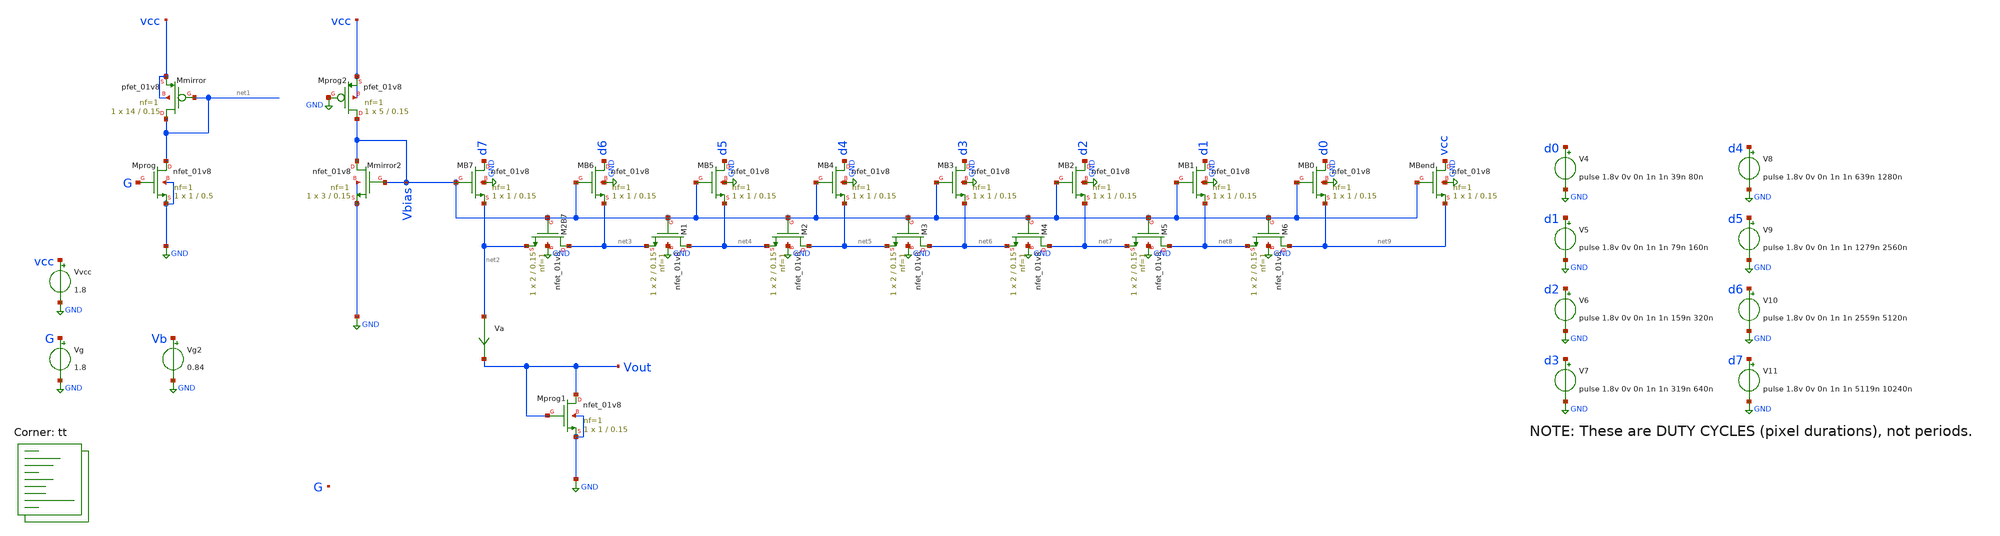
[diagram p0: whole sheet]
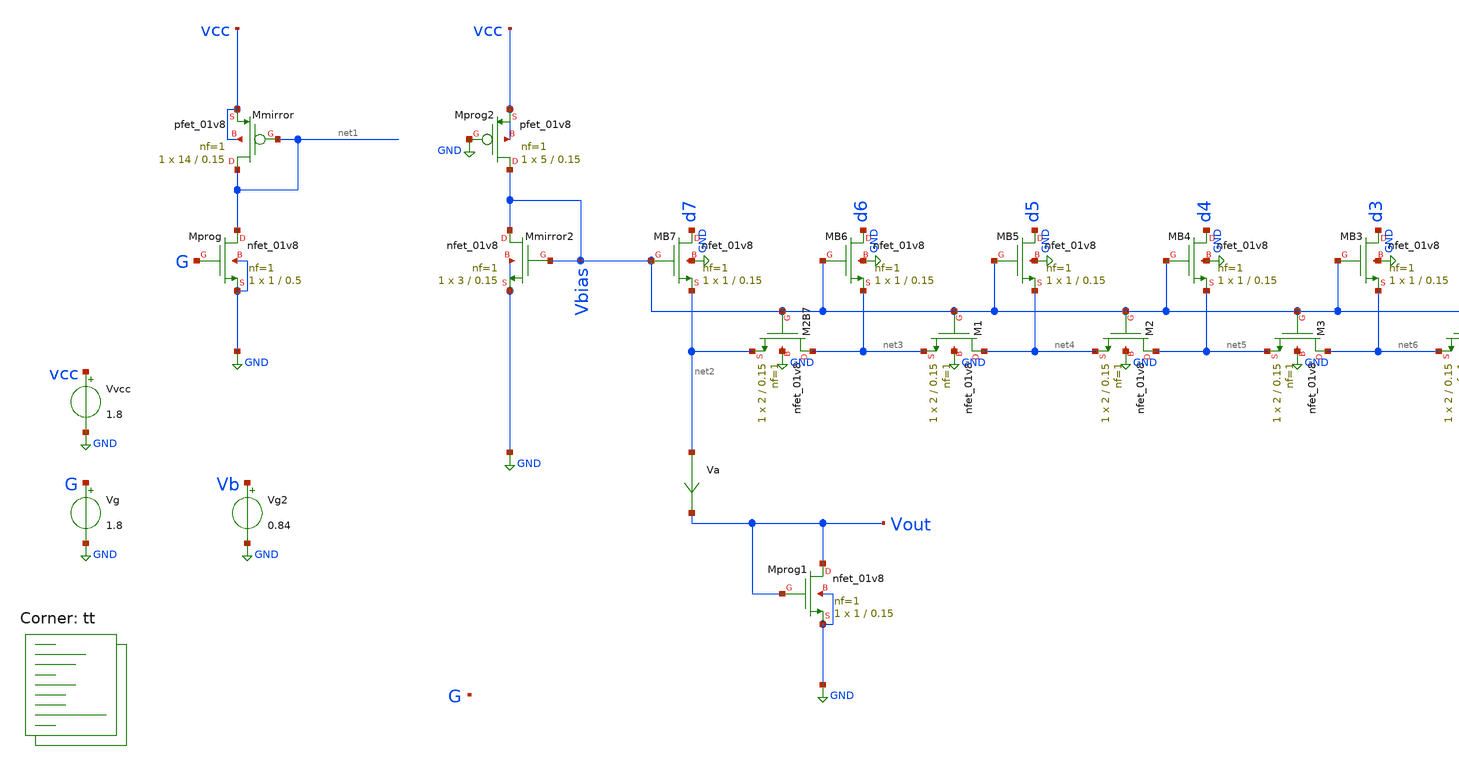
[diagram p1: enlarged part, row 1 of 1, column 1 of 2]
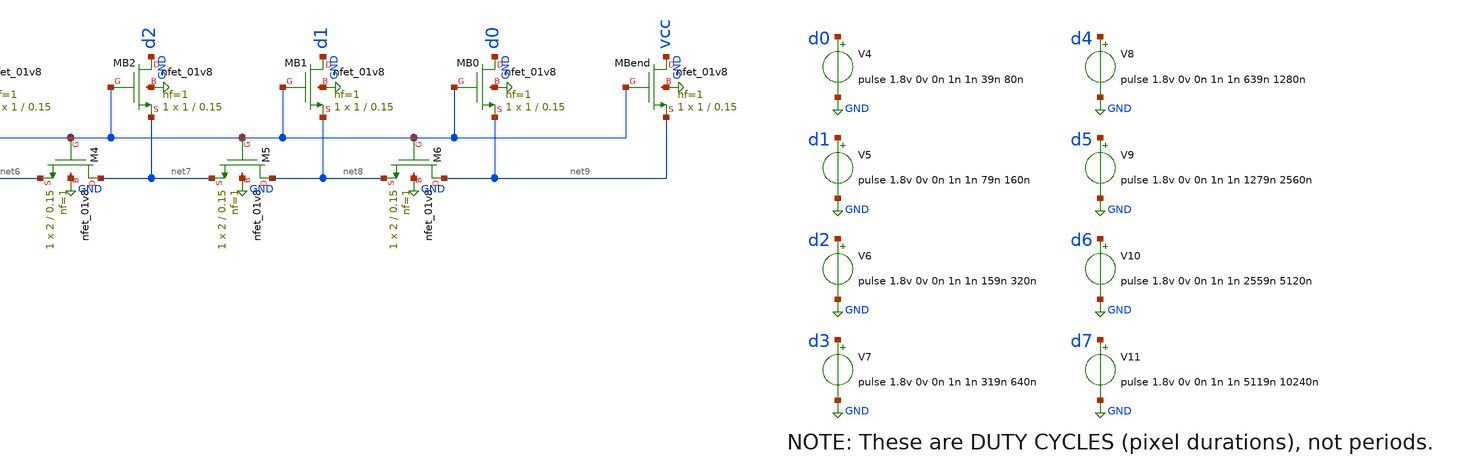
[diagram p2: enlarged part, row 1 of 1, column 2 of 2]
** sch_path: xschem/09-w2w.sch
**.subckt 09-w2w
Vvcc vcc GND 1.8
Vg2 Vb GND 0.84
Vg G GND 1.8
XMprog net1 G GND GND sky130_fd_pr__nfet_01v8 L=0.5 W=1 nf=1 ad='int((nf+1)/2) * W/nf * 0.29' as='int((nf+2)/2) * W/nf * 0.29'
+ pd='2*int((nf+1)/2) * (W/nf + 0.29)' ps='2*int((nf+2)/2) * (W/nf + 0.29)' nrd='0.29 / W' nrs='0.29 / W'
+ sa=0 sb=0 sd=0 mult=1 m=1
XMmirror net1 net1 vcc vcc sky130_fd_pr__pfet_01v8 L=0.15 W=14 nf=1 ad='int((nf+1)/2) * W/nf * 0.29'
+ as='int((nf+2)/2) * W/nf * 0.29' pd='2*int((nf+1)/2) * (W/nf + 0.29)' ps='2*int((nf+2)/2) * (W/nf + 0.29)'
+ nrd='0.29 / W' nrs='0.29 / W' sa=0 sb=0 sd=0 mult=1 m=1
XMprog2 Vbias GND vcc vcc sky130_fd_pr__pfet_01v8 L=0.15 W=5 nf=1 ad='int((nf+1)/2) * W/nf * 0.29' as='int((nf+2)/2) * W/nf * 0.29'
+ pd='2*int((nf+1)/2) * (W/nf + 0.29)' ps='2*int((nf+2)/2) * (W/nf + 0.29)' nrd='0.29 / W' nrs='0.29 / W'
+ sa=0 sb=0 sd=0 mult=1 m=1
XMmirror2 Vbias Vbias GND GND sky130_fd_pr__nfet_01v8 L=0.15 W=3 nf=1 ad='int((nf+1)/2) * W/nf * 0.29'
+ as='int((nf+2)/2) * W/nf * 0.29' pd='2*int((nf+1)/2) * (W/nf + 0.29)' ps='2*int((nf+2)/2) * (W/nf + 0.29)'
+ nrd='0.29 / W' nrs='0.29 / W' sa=0 sb=0 sd=0 mult=1 m=1
XMB7 d7 Vbias net2 GND sky130_fd_pr__nfet_01v8 L=0.15 W=1 nf=1 ad='int((nf+1)/2) * W/nf * 0.29' as='int((nf+2)/2) * W/nf * 0.29'
+ pd='2*int((nf+1)/2) * (W/nf + 0.29)' ps='2*int((nf+2)/2) * (W/nf + 0.29)' nrd='0.29 / W' nrs='0.29 / W'
+ sa=0 sb=0 sd=0 mult=1 m=1
XM2B7 net3 Vbias net2 GND sky130_fd_pr__nfet_01v8 L=0.15 W=2 nf=1 ad='int((nf+1)/2) * W/nf * 0.29' as='int((nf+2)/2) * W/nf * 0.29'
+ pd='2*int((nf+1)/2) * (W/nf + 0.29)' ps='2*int((nf+2)/2) * (W/nf + 0.29)' nrd='0.29 / W' nrs='0.29 / W'
+ sa=0 sb=0 sd=0 mult=1 m=1
XMB1 d1 Vbias net8 GND sky130_fd_pr__nfet_01v8 L=0.15 W=1 nf=1 ad='int((nf+1)/2) * W/nf * 0.29' as='int((nf+2)/2) * W/nf * 0.29'
+ pd='2*int((nf+1)/2) * (W/nf + 0.29)' ps='2*int((nf+2)/2) * (W/nf + 0.29)' nrd='0.29 / W' nrs='0.29 / W'
+ sa=0 sb=0 sd=0 mult=1 m=1
XM1 net4 Vbias net3 GND sky130_fd_pr__nfet_01v8 L=0.15 W=2 nf=1 ad='int((nf+1)/2) * W/nf * 0.29' as='int((nf+2)/2) * W/nf * 0.29'
+ pd='2*int((nf+1)/2) * (W/nf + 0.29)' ps='2*int((nf+2)/2) * (W/nf + 0.29)' nrd='0.29 / W' nrs='0.29 / W'
+ sa=0 sb=0 sd=0 mult=1 m=1
XMB2 d2 Vbias net7 GND sky130_fd_pr__nfet_01v8 L=0.15 W=1 nf=1 ad='int((nf+1)/2) * W/nf * 0.29' as='int((nf+2)/2) * W/nf * 0.29'
+ pd='2*int((nf+1)/2) * (W/nf + 0.29)' ps='2*int((nf+2)/2) * (W/nf + 0.29)' nrd='0.29 / W' nrs='0.29 / W'
+ sa=0 sb=0 sd=0 mult=1 m=1
XM2 net5 Vbias net4 GND sky130_fd_pr__nfet_01v8 L=0.15 W=2 nf=1 ad='int((nf+1)/2) * W/nf * 0.29' as='int((nf+2)/2) * W/nf * 0.29'
+ pd='2*int((nf+1)/2) * (W/nf + 0.29)' ps='2*int((nf+2)/2) * (W/nf + 0.29)' nrd='0.29 / W' nrs='0.29 / W'
+ sa=0 sb=0 sd=0 mult=1 m=1
XMB3 d3 Vbias net6 GND sky130_fd_pr__nfet_01v8 L=0.15 W=1 nf=1 ad='int((nf+1)/2) * W/nf * 0.29' as='int((nf+2)/2) * W/nf * 0.29'
+ pd='2*int((nf+1)/2) * (W/nf + 0.29)' ps='2*int((nf+2)/2) * (W/nf + 0.29)' nrd='0.29 / W' nrs='0.29 / W'
+ sa=0 sb=0 sd=0 mult=1 m=1
XM3 net6 Vbias net5 GND sky130_fd_pr__nfet_01v8 L=0.15 W=2 nf=1 ad='int((nf+1)/2) * W/nf * 0.29' as='int((nf+2)/2) * W/nf * 0.29'
+ pd='2*int((nf+1)/2) * (W/nf + 0.29)' ps='2*int((nf+2)/2) * (W/nf + 0.29)' nrd='0.29 / W' nrs='0.29 / W'
+ sa=0 sb=0 sd=0 mult=1 m=1
XMB4 d4 Vbias net5 GND sky130_fd_pr__nfet_01v8 L=0.15 W=1 nf=1 ad='int((nf+1)/2) * W/nf * 0.29' as='int((nf+2)/2) * W/nf * 0.29'
+ pd='2*int((nf+1)/2) * (W/nf + 0.29)' ps='2*int((nf+2)/2) * (W/nf + 0.29)' nrd='0.29 / W' nrs='0.29 / W'
+ sa=0 sb=0 sd=0 mult=1 m=1
XM4 net7 Vbias net6 GND sky130_fd_pr__nfet_01v8 L=0.15 W=2 nf=1 ad='int((nf+1)/2) * W/nf * 0.29' as='int((nf+2)/2) * W/nf * 0.29'
+ pd='2*int((nf+1)/2) * (W/nf + 0.29)' ps='2*int((nf+2)/2) * (W/nf + 0.29)' nrd='0.29 / W' nrs='0.29 / W'
+ sa=0 sb=0 sd=0 mult=1 m=1
XMB5 d5 Vbias net4 GND sky130_fd_pr__nfet_01v8 L=0.15 W=1 nf=1 ad='int((nf+1)/2) * W/nf * 0.29' as='int((nf+2)/2) * W/nf * 0.29'
+ pd='2*int((nf+1)/2) * (W/nf + 0.29)' ps='2*int((nf+2)/2) * (W/nf + 0.29)' nrd='0.29 / W' nrs='0.29 / W'
+ sa=0 sb=0 sd=0 mult=1 m=1
XM5 net8 Vbias net7 GND sky130_fd_pr__nfet_01v8 L=0.15 W=2 nf=1 ad='int((nf+1)/2) * W/nf * 0.29' as='int((nf+2)/2) * W/nf * 0.29'
+ pd='2*int((nf+1)/2) * (W/nf + 0.29)' ps='2*int((nf+2)/2) * (W/nf + 0.29)' nrd='0.29 / W' nrs='0.29 / W'
+ sa=0 sb=0 sd=0 mult=1 m=1
XMB6 d6 Vbias net3 GND sky130_fd_pr__nfet_01v8 L=0.15 W=1 nf=1 ad='int((nf+1)/2) * W/nf * 0.29' as='int((nf+2)/2) * W/nf * 0.29'
+ pd='2*int((nf+1)/2) * (W/nf + 0.29)' ps='2*int((nf+2)/2) * (W/nf + 0.29)' nrd='0.29 / W' nrs='0.29 / W'
+ sa=0 sb=0 sd=0 mult=1 m=1
XM6 net9 Vbias net8 GND sky130_fd_pr__nfet_01v8 L=0.15 W=2 nf=1 ad='int((nf+1)/2) * W/nf * 0.29' as='int((nf+2)/2) * W/nf * 0.29'
+ pd='2*int((nf+1)/2) * (W/nf + 0.29)' ps='2*int((nf+2)/2) * (W/nf + 0.29)' nrd='0.29 / W' nrs='0.29 / W'
+ sa=0 sb=0 sd=0 mult=1 m=1
XMB0 d0 Vbias net9 GND sky130_fd_pr__nfet_01v8 L=0.15 W=1 nf=1 ad='int((nf+1)/2) * W/nf * 0.29' as='int((nf+2)/2) * W/nf * 0.29'
+ pd='2*int((nf+1)/2) * (W/nf + 0.29)' ps='2*int((nf+2)/2) * (W/nf + 0.29)' nrd='0.29 / W' nrs='0.29 / W'
+ sa=0 sb=0 sd=0 mult=1 m=1
XMBend vcc Vbias net9 GND sky130_fd_pr__nfet_01v8 L=0.15 W=1 nf=1 ad='int((nf+1)/2) * W/nf * 0.29' as='int((nf+2)/2) * W/nf * 0.29'
+ pd='2*int((nf+1)/2) * (W/nf + 0.29)' ps='2*int((nf+2)/2) * (W/nf + 0.29)' nrd='0.29 / W' nrs='0.29 / W'
+ sa=0 sb=0 sd=0 mult=1 m=1
Va net2 Vout 0
.save i(va)
V4 d0 GND pulse 1.8v 0v 0n 1n 1n 39n 80n
V5 d1 GND pulse 1.8v 0v 0n 1n 1n 79n 160n
V6 d2 GND pulse 1.8v 0v 0n 1n 1n 159n 320n
V7 d3 GND pulse 1.8v 0v 0n 1n 1n 319n 640n
V8 d4 GND pulse 1.8v 0v 0n 1n 1n 639n 1280n
V9 d5 GND pulse 1.8v 0v 0n 1n 1n 1279n 2560n
V10 d6 GND pulse 1.8v 0v 0n 1n 1n 2559n 5120n
V11 d7 GND pulse 1.8v 0v 0n 1n 1n 5119n 10240n
XMprog1 Vout Vout GND GND sky130_fd_pr__nfet_01v8 L=0.15 W=1 nf=1 ad='int((nf+1)/2) * W/nf * 0.29' as='int((nf+2)/2) * W/nf * 0.29'
+ pd='2*int((nf+1)/2) * (W/nf + 0.29)' ps='2*int((nf+2)/2) * (W/nf + 0.29)' nrd='0.29 / W' nrs='0.29 / W'
+ sa=0 sb=0 sd=0 mult=1 m=1
**** begin user architecture code



.options savecurrents
.control

  save all
  tran 1n 12.8u
  *write 09.raw v(Vb) i(va1) i(va2) i(va3) i(va4) i(va5)
  *plot i(va1) i(va2) i(va3) i(va4) i(va5)
  plot vout
  plot i(va)

.endc



.lib $::SKYWATER_MODELS/sky130.lib.spice tt
**** end user architecture code
**.ends
.GLOBAL GND
.end
